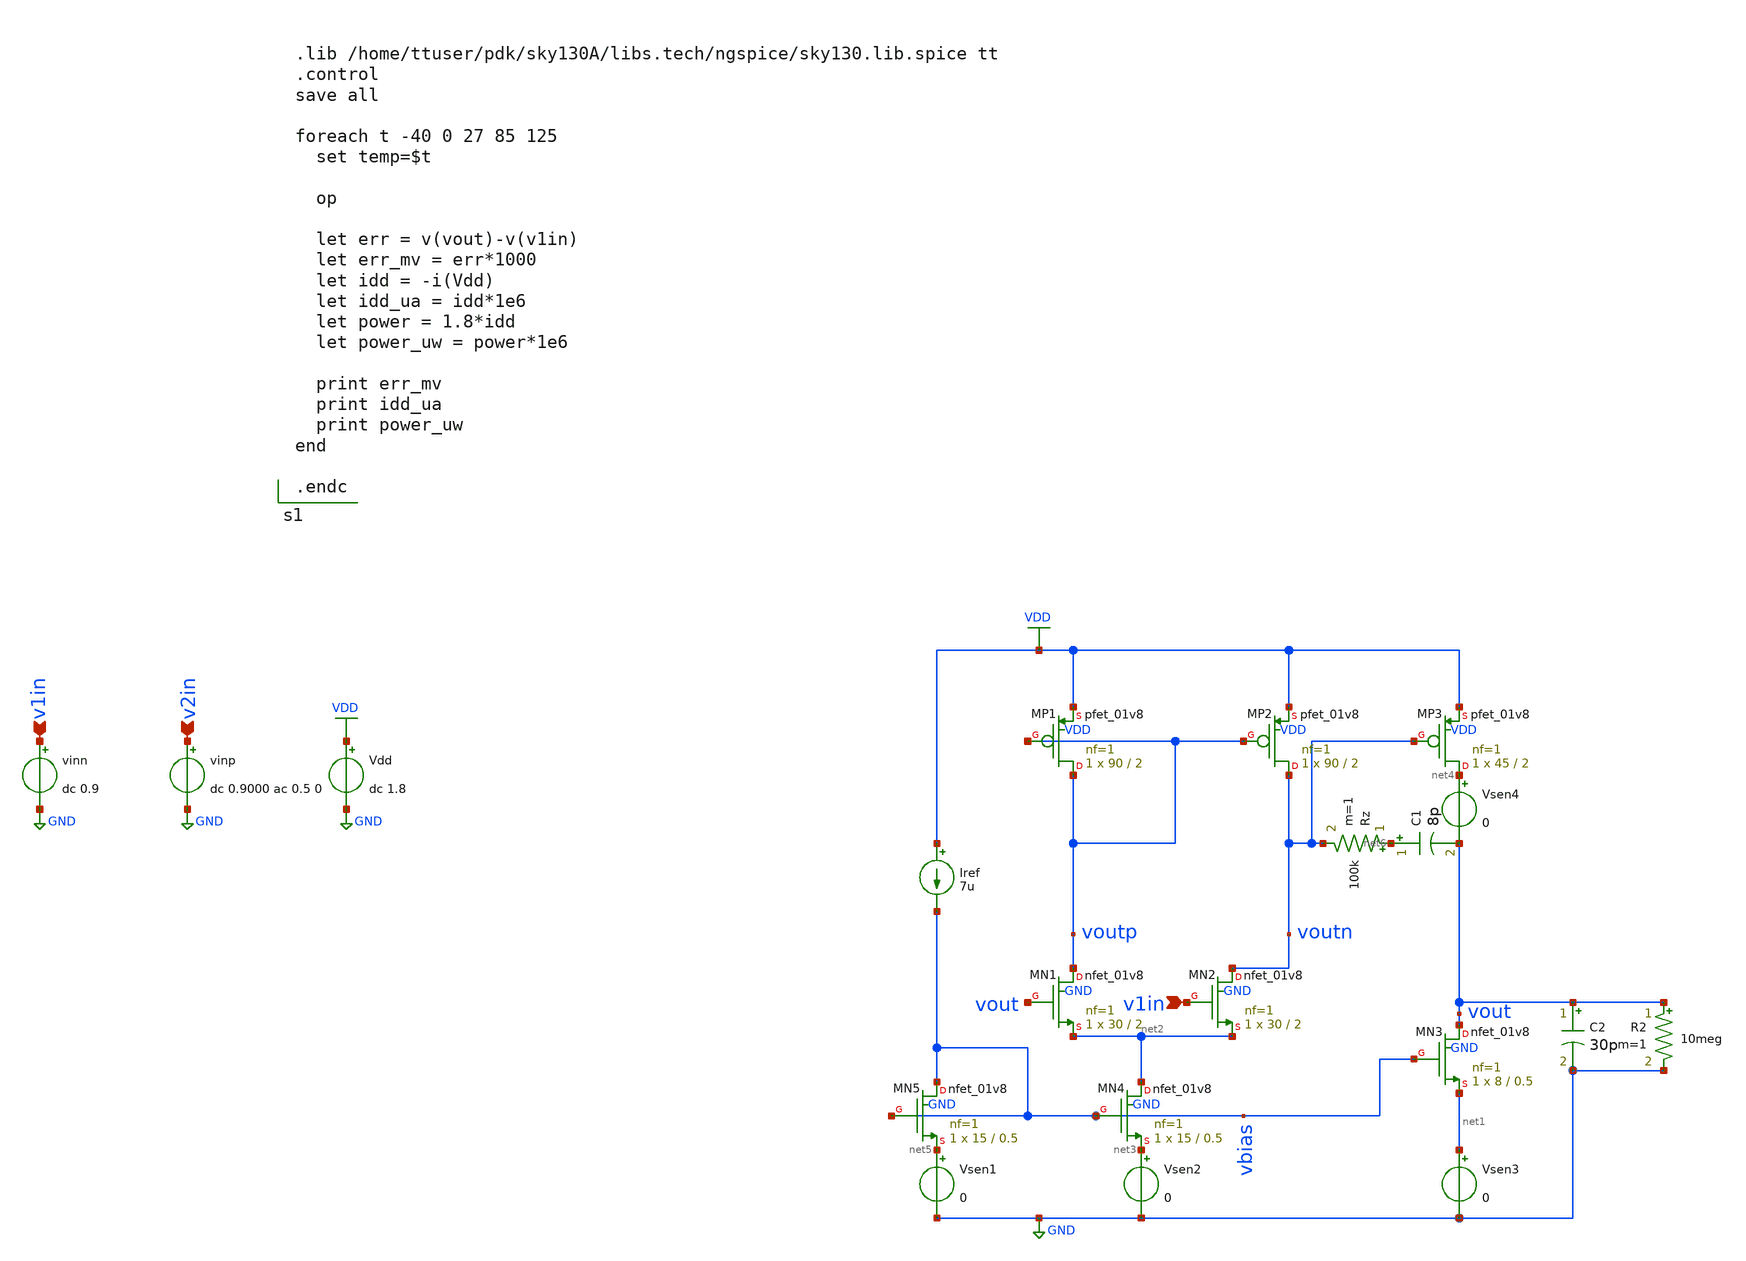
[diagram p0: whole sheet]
** sch_path: testbenches/prelayout/tempSweep.sch
**.subckt tempSweep v1in v1in v2in
*.ipin v1in
*.ipin v1in
*.ipin v2in
Vdd VDD GND dc 1.8
vinp v2in GND dc 0.9000 ac 0.5 0
vinn v1in GND dc 0.9
XMN1 voutp vout net2 GND sky130_fd_pr__nfet_01v8 L=2 W=30 nf=1 ad='int((nf+1)/2) * W/nf * 0.29' as='int((nf+2)/2) * W/nf * 0.29'
+ pd='2*int((nf+1)/2) * (W/nf + 0.29)' ps='2*int((nf+2)/2) * (W/nf + 0.29)' nrd='0.29 / W' nrs='0.29 / W'
+ sa=0 sb=0 sd=0 mult=1 m=1
XMN2 voutn v1in net2 GND sky130_fd_pr__nfet_01v8 L=2 W=30 nf=1 ad='int((nf+1)/2) * W/nf * 0.29' as='int((nf+2)/2) * W/nf * 0.29'
+ pd='2*int((nf+1)/2) * (W/nf + 0.29)' ps='2*int((nf+2)/2) * (W/nf + 0.29)' nrd='0.29 / W' nrs='0.29 / W'
+ sa=0 sb=0 sd=0 mult=1 m=1
XMP1 voutp voutp VDD VDD sky130_fd_pr__pfet_01v8 L=2 W=90 nf=1 ad='int((nf+1)/2) * W/nf * 0.29' as='int((nf+2)/2) * W/nf * 0.29'
+ pd='2*int((nf+1)/2) * (W/nf + 0.29)' ps='2*int((nf+2)/2) * (W/nf + 0.29)' nrd='0.29 / W' nrs='0.29 / W'
+ sa=0 sb=0 sd=0 mult=1 m=1
XMP2 voutn voutp VDD VDD sky130_fd_pr__pfet_01v8 L=2 W=90 nf=1 ad='int((nf+1)/2) * W/nf * 0.29' as='int((nf+2)/2) * W/nf * 0.29'
+ pd='2*int((nf+1)/2) * (W/nf + 0.29)' ps='2*int((nf+2)/2) * (W/nf + 0.29)' nrd='0.29 / W' nrs='0.29 / W'
+ sa=0 sb=0 sd=0 mult=1 m=1
Iref VDD vbias 7u
Vsen2 net3 GND 0
XMP3 net4 voutn VDD VDD sky130_fd_pr__pfet_01v8 L=2 W=45 nf=1 ad='int((nf+1)/2) * W/nf * 0.29' as='int((nf+2)/2) * W/nf * 0.29'
+ pd='2*int((nf+1)/2) * (W/nf + 0.29)' ps='2*int((nf+2)/2) * (W/nf + 0.29)' nrd='0.29 / W' nrs='0.29 / W'
+ sa=0 sb=0 sd=0 mult=1 m=1
XMN3 vout vbias net1 GND sky130_fd_pr__nfet_01v8 L=0.5 W=8 nf=1 ad='int((nf+1)/2) * W/nf * 0.29' as='int((nf+2)/2) * W/nf * 0.29'
+ pd='2*int((nf+1)/2) * (W/nf + 0.29)' ps='2*int((nf+2)/2) * (W/nf + 0.29)' nrd='0.29 / W' nrs='0.29 / W'
+ sa=0 sb=0 sd=0 mult=1 m=1
Vsen3 net1 GND 0
Vsen1 net5 GND 0
C1 net6 vout 8p m=1
XMN4 net2 vbias net3 GND sky130_fd_pr__nfet_01v8 L=0.5 W=15 nf=1 ad='int((nf+1)/2) * W/nf * 0.29' as='int((nf+2)/2) * W/nf * 0.29'
+ pd='2*int((nf+1)/2) * (W/nf + 0.29)' ps='2*int((nf+2)/2) * (W/nf + 0.29)' nrd='0.29 / W' nrs='0.29 / W'
+ sa=0 sb=0 sd=0 mult=1 m=1
XMN5 vbias vbias net5 GND sky130_fd_pr__nfet_01v8 L=0.5 W=15 nf=1 ad='int((nf+1)/2) * W/nf * 0.29' as='int((nf+2)/2) * W/nf * 0.29'
+ pd='2*int((nf+1)/2) * (W/nf + 0.29)' ps='2*int((nf+2)/2) * (W/nf + 0.29)' nrd='0.29 / W' nrs='0.29 / W'
+ sa=0 sb=0 sd=0 mult=1 m=1
C2 vout GND 30p m=1
Rz net6 voutn 100k m=1
Vsen4 net4 vout 0
R2 vout GND 10meg m=1
**** begin user architecture code


.lib /home/ttuser/pdk/sky130A/libs.tech/ngspice/sky130.lib.spice tt
.control
save all

foreach t -40 0 27 85 125
  set temp=$t

  op

  let err = v(vout)-v(v1in)
  let err_mv = err*1000
  let idd = -i(Vdd)
  let idd_ua = idd*1e6
  let power = 1.8*idd
  let power_uw = power*1e6

  print err_mv
  print idd_ua
  print power_uw
end

.endc


**** end user architecture code
**.ends
.GLOBAL VDD
.GLOBAL GND
.end
